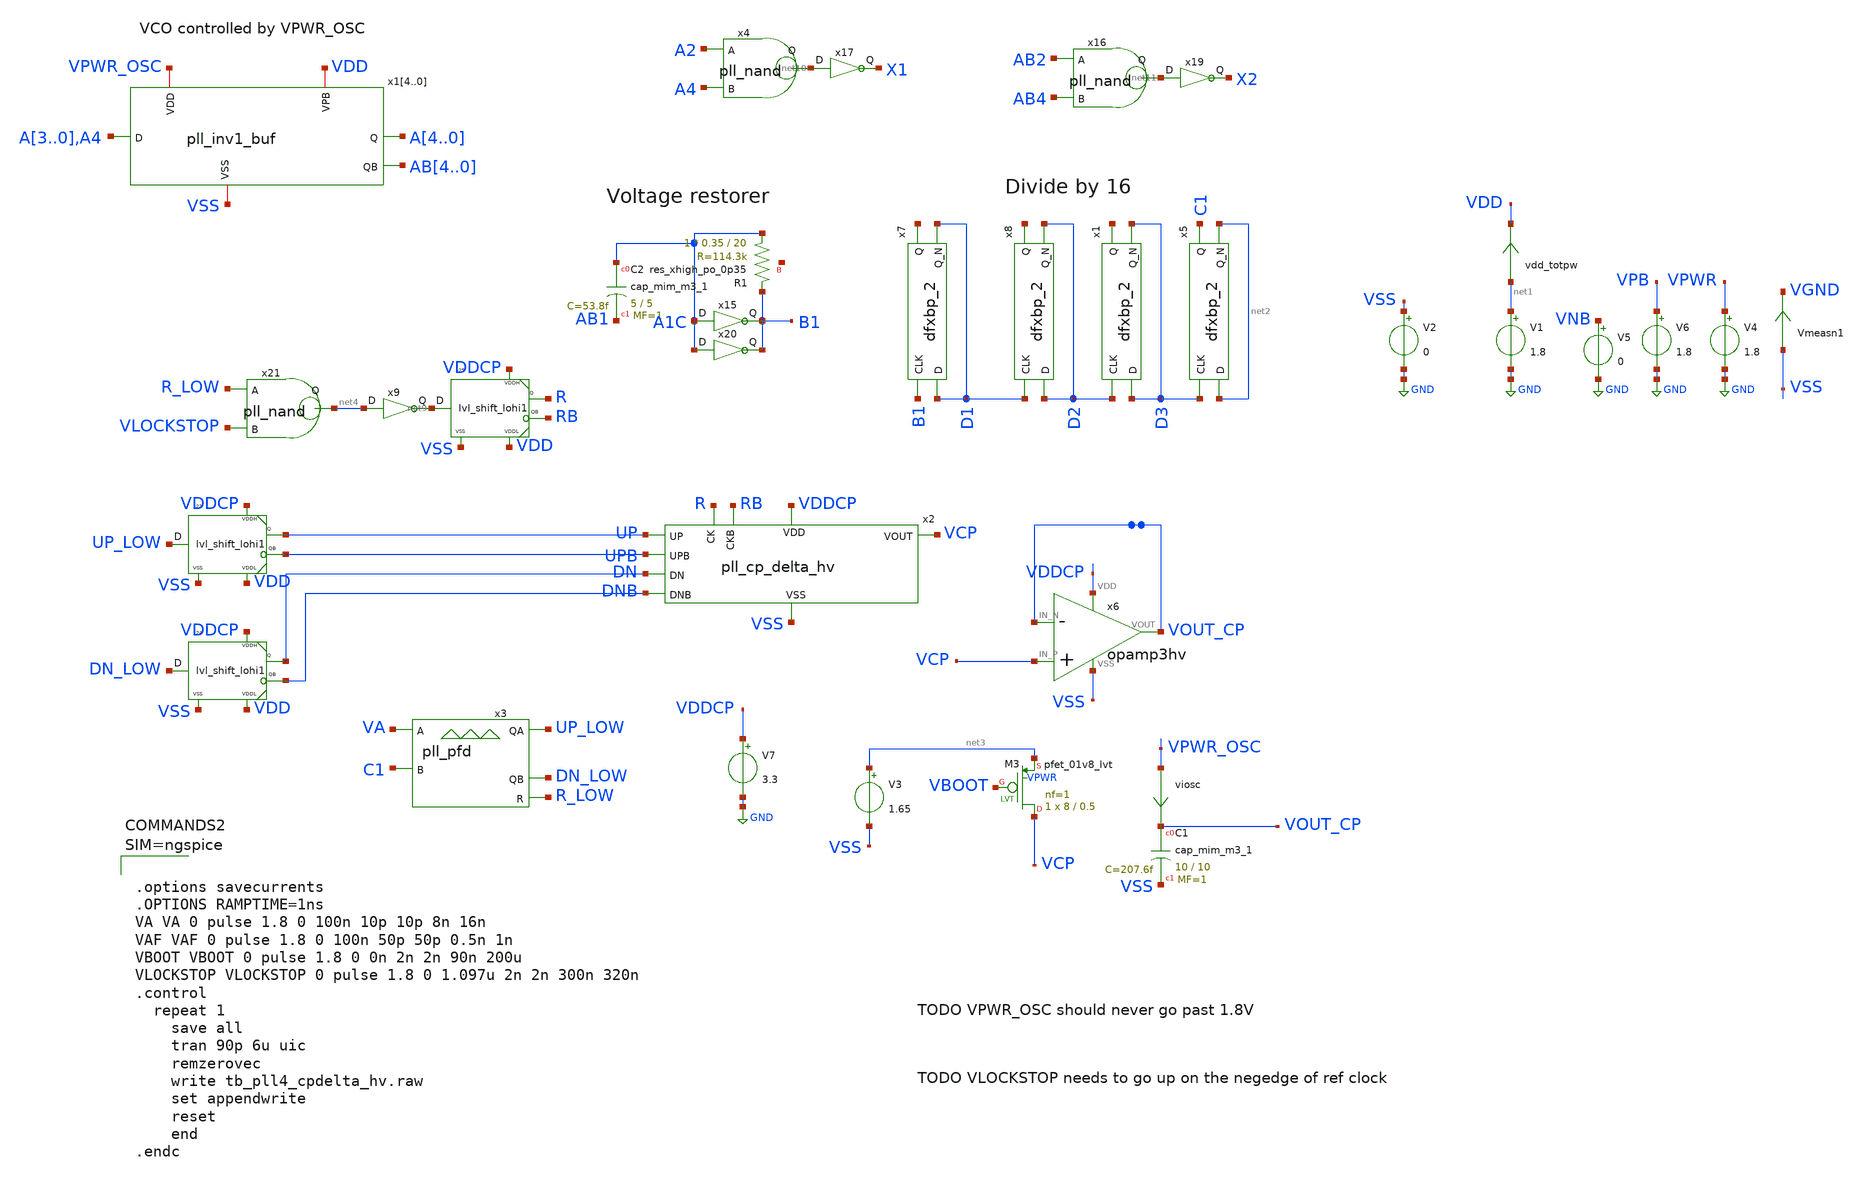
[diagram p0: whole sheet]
** sch_path: xschem/tb_pll4_cpdelta_hv.sch
**.subckt tb_pll4_cpdelta_hv
V5 VNB GND 0
V6 VPB GND 1.8
V1 net1 GND 1.8
V2 VSS GND 0
vdd_totpw net1 VDD 0
.save i(vdd_totpw)
Vmeasn1 VSS VGND 0
.save i(vmeasn1)
x3 VA C1 UP_LOW DN_LOW R_LOW VDD VSS pll_pfd
x7 B1 D1 VGND VNB VPB VPWR net5 D1 sky130_fd_sc_hd__dfxbp_2
x8 D1 D2 VGND VNB VPB VPWR net6 D2 sky130_fd_sc_hd__dfxbp_2
V4 VPWR GND 1.8
x1 D2 D3 VGND VNB VPB VPWR net7 D3 sky130_fd_sc_hd__dfxbp_2
x5 D3 net2 VGND VNB VPB VPWR C1 net2 sky130_fd_sc_hd__dfxbp_2
V7 VDDCP GND 3.3
x15 A1C B1 VDD VSS pll_inv1
XR1 A1C B1 net8 sky130_fd_pr__res_xhigh_po_0p35 L=20 mult=1 m=1
XC2 A1C AB1 sky130_fd_pr__cap_mim_m3_1 W=5 L=5 MF=1 m=1
viosc VPWR_OSC VOUT_CP 0
.save i(viosc)
V3 net3 VSS 1.65
x6 VDDCP VCP VOUT_CP VOUT_CP VSS opamp3hv
x2 VDDCP UP DN VCP VSS UPB DNB R RB pll_cp_delta_hv
x23 UP_LOW UP UPB VDDCP VDD VSS lvl_shift_lohi1
x24 DN_LOW DN DNB VDDCP VDD VSS lvl_shift_lohi1
x25 net9 R RB VDDCP VDD VSS lvl_shift_lohi1
x9 net4 net9 VDD VSS pll_inv1
XC1 VOUT_CP VSS sky130_fd_pr__cap_mim_m3_1 W=10 L=10 MF=1 m=1
XM3 VCP VBOOT net3 VPWR sky130_fd_pr__pfet_01v8_lvt L=0.5 W=8 nf=1 ad='int((nf+1)/2) * W/nf * 0.29' as='int((nf+2)/2) * W/nf * 0.29'
+ pd='2*int((nf+1)/2) * (W/nf + 0.29)' ps='2*int((nf+2)/2) * (W/nf + 0.29)' nrd='0.29 / W' nrs='0.29 / W'
+ sa=0 sb=0 sd=0 mult=1 m=1
x14 A3 A4 AB4 VDD VPWR_OSC VSS pll_inv1_buf
x13 A2 A3 AB3 VDD VPWR_OSC VSS pll_inv1_buf
x12 A1 A2 AB2 VDD VPWR_OSC VSS pll_inv1_buf
x11 A0 A1 AB1 VDD VPWR_OSC VSS pll_inv1_buf
x10 A4 A0 AB0 VDD VPWR_OSC VSS pll_inv1_buf
x17 net10 X1 VDD VSS pll_inv1
x19 net11 X2 VDD VSS pll_inv1
x20 A1C B1 VDD VSS pll_inv1
x21 R_LOW VLOCKSTOP net4 VSS VDD pll_nand
x4 A2 A4 net10 VSS VDD pll_nand
x16 AB2 AB4 net11 VSS VDD pll_nand
**** begin user architecture code

** opencircuitdesign pdks install
.lib $::SKYWATER_MODELS/sky130.lib.spice tt_mm
.include $::SKYWATER_STDCELLS/sky130_fd_sc_hd.spice





.options savecurrents
.OPTIONS RAMPTIME=1ns
VA VA 0 pulse 1.8 0 100n 10p 10p 8n 16n
VAF VAF 0 pulse 1.8 0 100n 50p 50p 0.5n 1n
VBOOT VBOOT 0 pulse 1.8 0 0n 2n 2n 90n 200u
VLOCKSTOP VLOCKSTOP 0 pulse 1.8 0 1.097u 2n 2n 300n 320n
.control
  repeat 1
    save all
    tran 90p 6u uic
    remzerovec
    write tb_pll4_cpdelta_hv.raw
    set appendwrite
    reset
    end
.endc



**** end user architecture code
**.ends
.GLOBAL GND
.end
